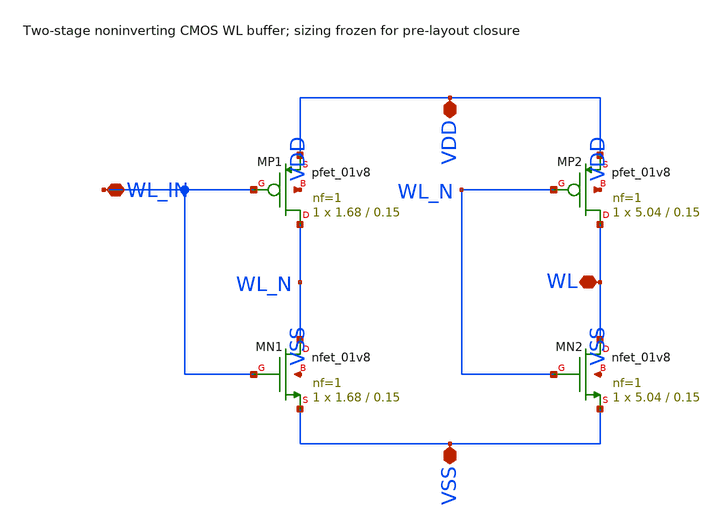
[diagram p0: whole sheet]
** sch_path: sims/integration/results/reconciliation_20261030/physical/cells/wl_driver/wl_driver.sch
**.subckt wl_driver VDD VSS WL_IN WL
*.iopin VDD
*.iopin VSS
*.iopin WL_IN
*.iopin WL
XMP1 WL_N WL_IN VDD VDD sky130_fd_pr__pfet_01v8 L=0.15 W=1.68 nf=1 ad='int((nf+1)/2) * W/nf * 0.29' as='int((nf+2)/2) * W/nf * 0.29'
+ pd='2*int((nf+1)/2) * (W/nf + 0.29)' ps='2*int((nf+2)/2) * (W/nf + 0.29)' nrd='0.29 / W' nrs='0.29 / W'
+ sa=0 sb=0 sd=0 mult=1 m=1
XMN1 WL_N WL_IN VSS VSS sky130_fd_pr__nfet_01v8 L=0.15 W=1.68 nf=1 ad='int((1 + 1)/2) * 1.68 / 1 * 0.29'
+ as='int((1 + 2)/2) * 1.68 / 1 * 0.29' pd='2*int((1 + 1)/2) * (1.68 / 1 + 0.29)' ps='2*int((1 + 2)/2) * (1.68 / 1 + 0.29)'
+ nrd='0.29 / 1.68 ' nrs='0.29 / 1.68 ' sa=0 sb=0 sd=0 mult=1 m=1
XMP2 WL WL_N VDD VDD sky130_fd_pr__pfet_01v8 L=0.15 W=5.04 nf=1 ad='int((nf+1)/2) * W/nf * 0.29' as='int((nf+2)/2) * W/nf * 0.29'
+ pd='2*int((nf+1)/2) * (W/nf + 0.29)' ps='2*int((nf+2)/2) * (W/nf + 0.29)' nrd='0.29 / W' nrs='0.29 / W'
+ sa=0 sb=0 sd=0 mult=1 m=1
XMN2 WL WL_N VSS VSS sky130_fd_pr__nfet_01v8 L=0.15 W=5.04 nf=1 ad='int((1 + 1)/2) * 5.04 / 1 * 0.29'
+ as='int((1 + 2)/2) * 5.04 / 1 * 0.29' pd='2*int((1 + 1)/2) * (5.04 / 1 + 0.29)' ps='2*int((1 + 2)/2) * (5.04 / 1 + 0.29)'
+ nrd='0.29 / 5.04 ' nrs='0.29 / 5.04 ' sa=0 sb=0 sd=0 mult=1 m=1
**.ends
.end
